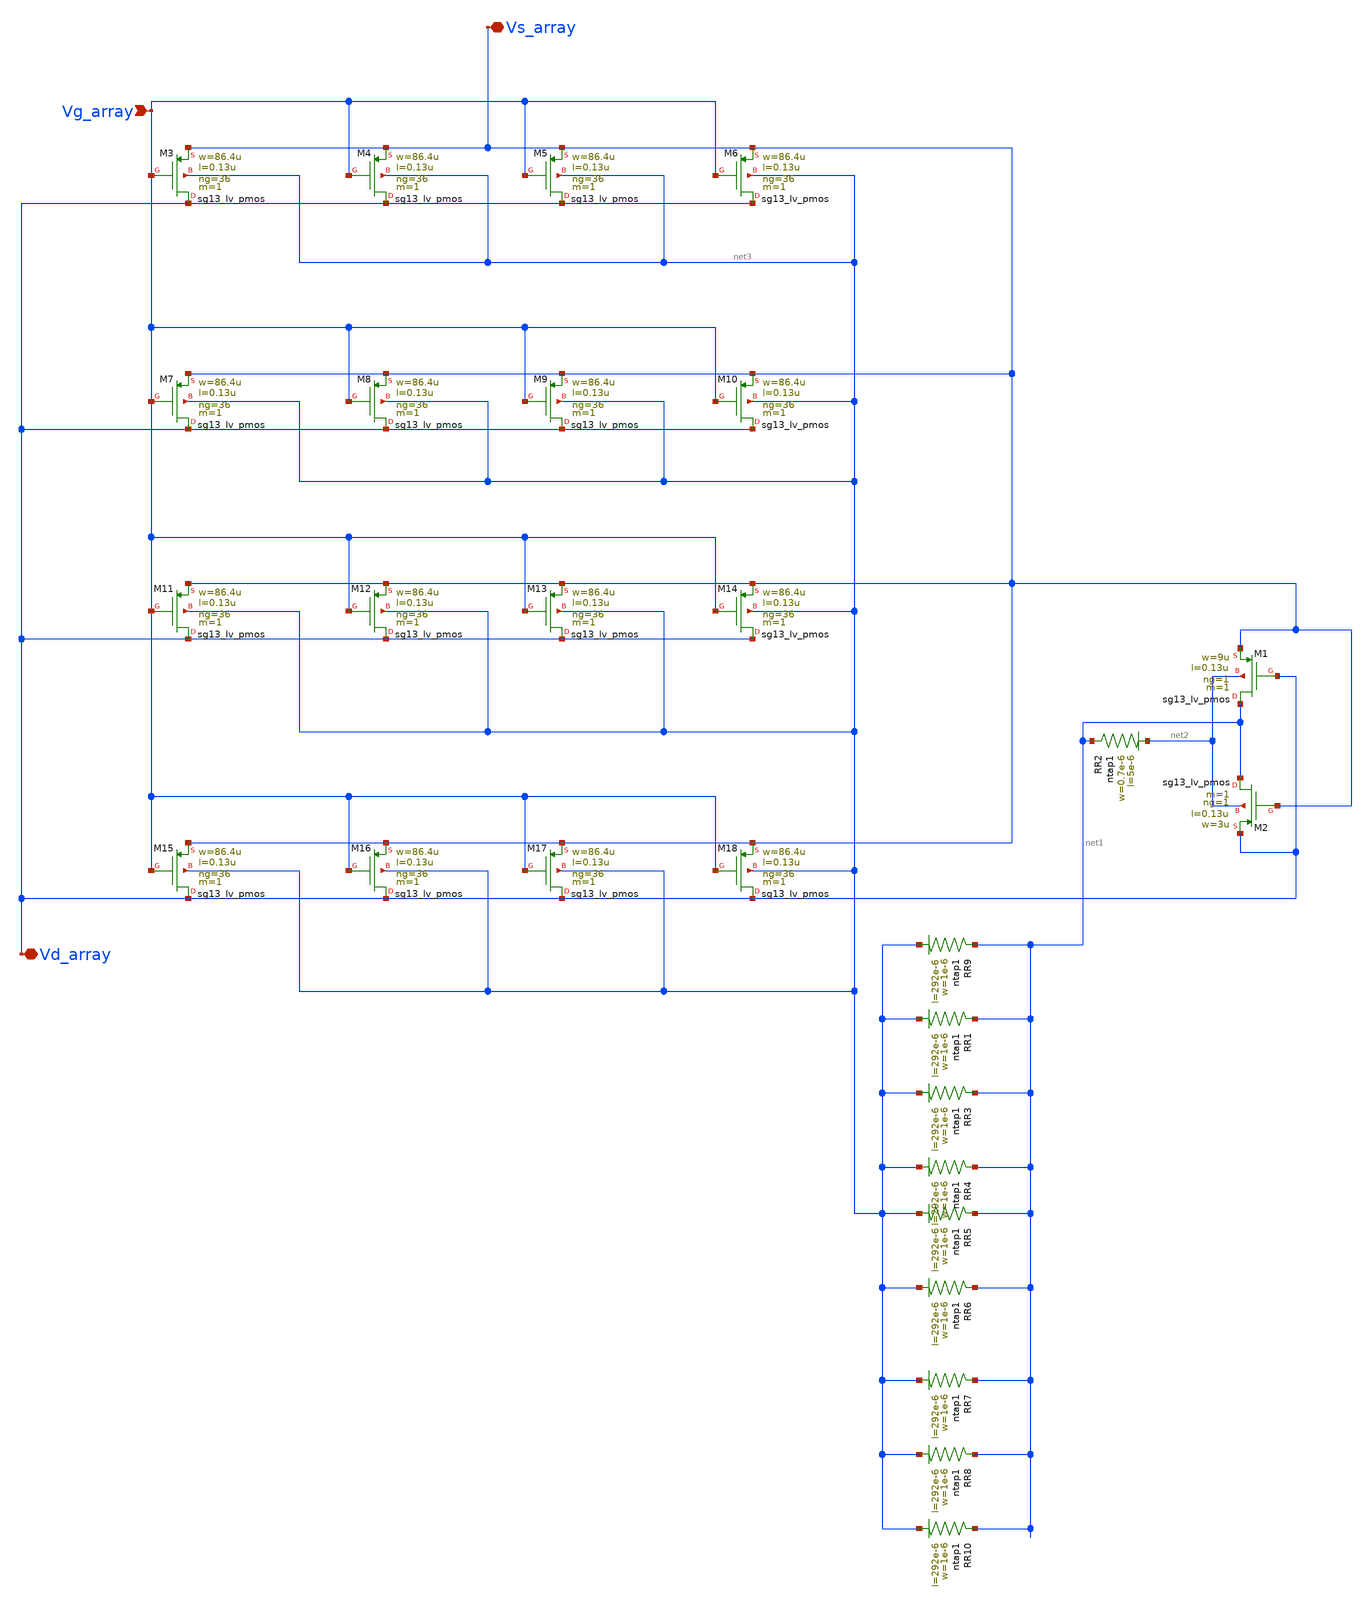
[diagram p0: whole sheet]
** sch_path: Layouts/PMOS/pmos_body_bias.sch
**.subckt pmos_body_bias Vg_array Vs_array Vd_array
*.ipin Vg_array
*.iopin Vs_array
*.iopin Vd_array
XM1 net1 Vd_array Vs_array net2 sg13_lv_pmos w=9u l=0.13u ng=1 m=1 mm_ok=1
XM2 net1 Vs_array Vd_array net2 sg13_lv_pmos w=3u l=0.13u ng=1 m=1 mm_ok=1
XR2 net1 net2 ntap1 R=65.77 w=0.7e-6 l=5e-6
XM3 Vd_array Vg_array Vs_array net3 sg13_lv_pmos w=86.4u l=0.13u ng=36 m=1 mm_ok=1
XM4 Vd_array Vg_array Vs_array net3 sg13_lv_pmos w=86.4u l=0.13u ng=36 m=1 mm_ok=1
XM5 Vd_array Vg_array Vs_array net3 sg13_lv_pmos w=86.4u l=0.13u ng=36 m=1 mm_ok=1
XM6 Vd_array Vg_array Vs_array net3 sg13_lv_pmos w=86.4u l=0.13u ng=36 m=1 mm_ok=1
XM7 Vd_array Vg_array Vs_array net3 sg13_lv_pmos w=86.4u l=0.13u ng=36 m=1 mm_ok=1
XM8 Vd_array Vg_array Vs_array net3 sg13_lv_pmos w=86.4u l=0.13u ng=36 m=1 mm_ok=1
XM9 Vd_array Vg_array Vs_array net3 sg13_lv_pmos w=86.4u l=0.13u ng=36 m=1 mm_ok=1
XM10 Vd_array Vg_array Vs_array net3 sg13_lv_pmos w=86.4u l=0.13u ng=36 m=1 mm_ok=1
XM11 Vd_array Vg_array Vs_array net3 sg13_lv_pmos w=86.4u l=0.13u ng=36 m=1 mm_ok=1
XM12 Vd_array Vg_array Vs_array net3 sg13_lv_pmos w=86.4u l=0.13u ng=36 m=1 mm_ok=1
XM13 Vd_array Vg_array Vs_array net3 sg13_lv_pmos w=86.4u l=0.13u ng=36 m=1 mm_ok=1
XM14 Vd_array Vg_array Vs_array net3 sg13_lv_pmos w=86.4u l=0.13u ng=36 m=1 mm_ok=1
XM15 Vd_array Vg_array Vs_array net3 sg13_lv_pmos w=86.4u l=0.13u ng=36 m=1 mm_ok=1
XM16 Vd_array Vg_array Vs_array net3 sg13_lv_pmos w=86.4u l=0.13u ng=36 m=1 mm_ok=1
XM17 Vd_array Vg_array Vs_array net3 sg13_lv_pmos w=86.4u l=0.13u ng=36 m=1 mm_ok=1
XM18 Vd_array Vg_array Vs_array net3 sg13_lv_pmos w=86.4u l=0.13u ng=36 m=1 mm_ok=1
XR9 net1 net3 ntap1 R=1.116 w=1e-6 l=292e-6
XR1 net1 net3 ntap1 R=1.116 w=1e-6 l=292e-6
XR3 net1 net3 ntap1 R=1.116 w=1e-6 l=292e-6
XR4 net1 net3 ntap1 R=1.116 w=1e-6 l=292e-6
XR5 net1 net3 ntap1 R=1.116 w=1e-6 l=292e-6
XR6 net1 net3 ntap1 R=1.116 w=1e-6 l=292e-6
XR7 net1 net3 ntap1 R=1.116 w=1e-6 l=292e-6
XR8 net1 net3 ntap1 R=1.116 w=1e-6 l=292e-6
XR10 net1 net3 ntap1 R=1.116 w=1e-6 l=292e-6
**.ends
.end
